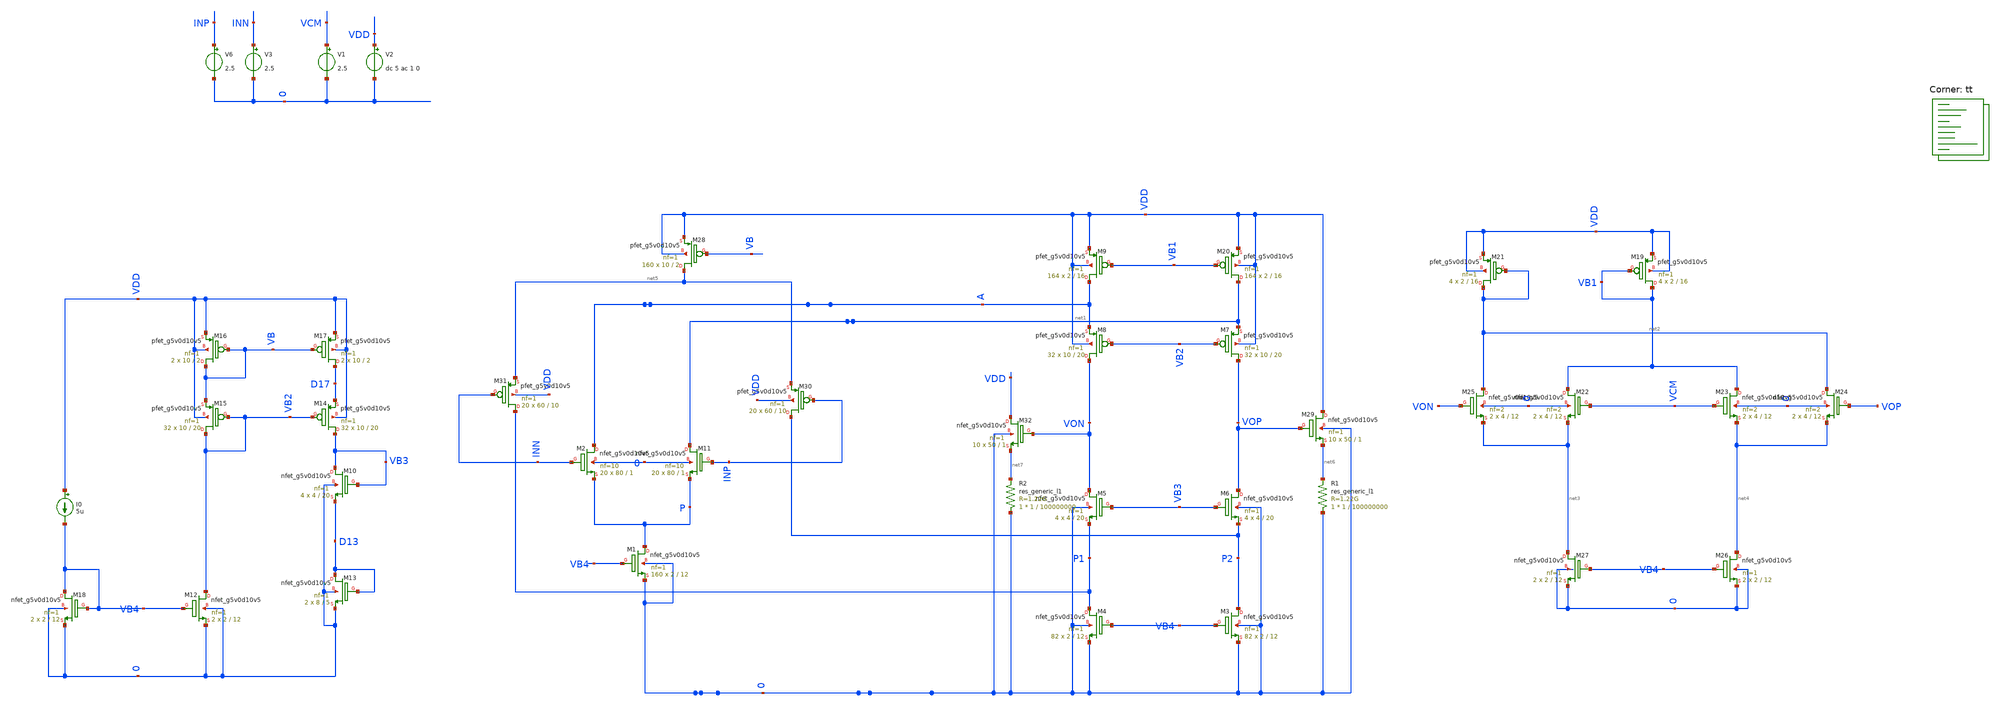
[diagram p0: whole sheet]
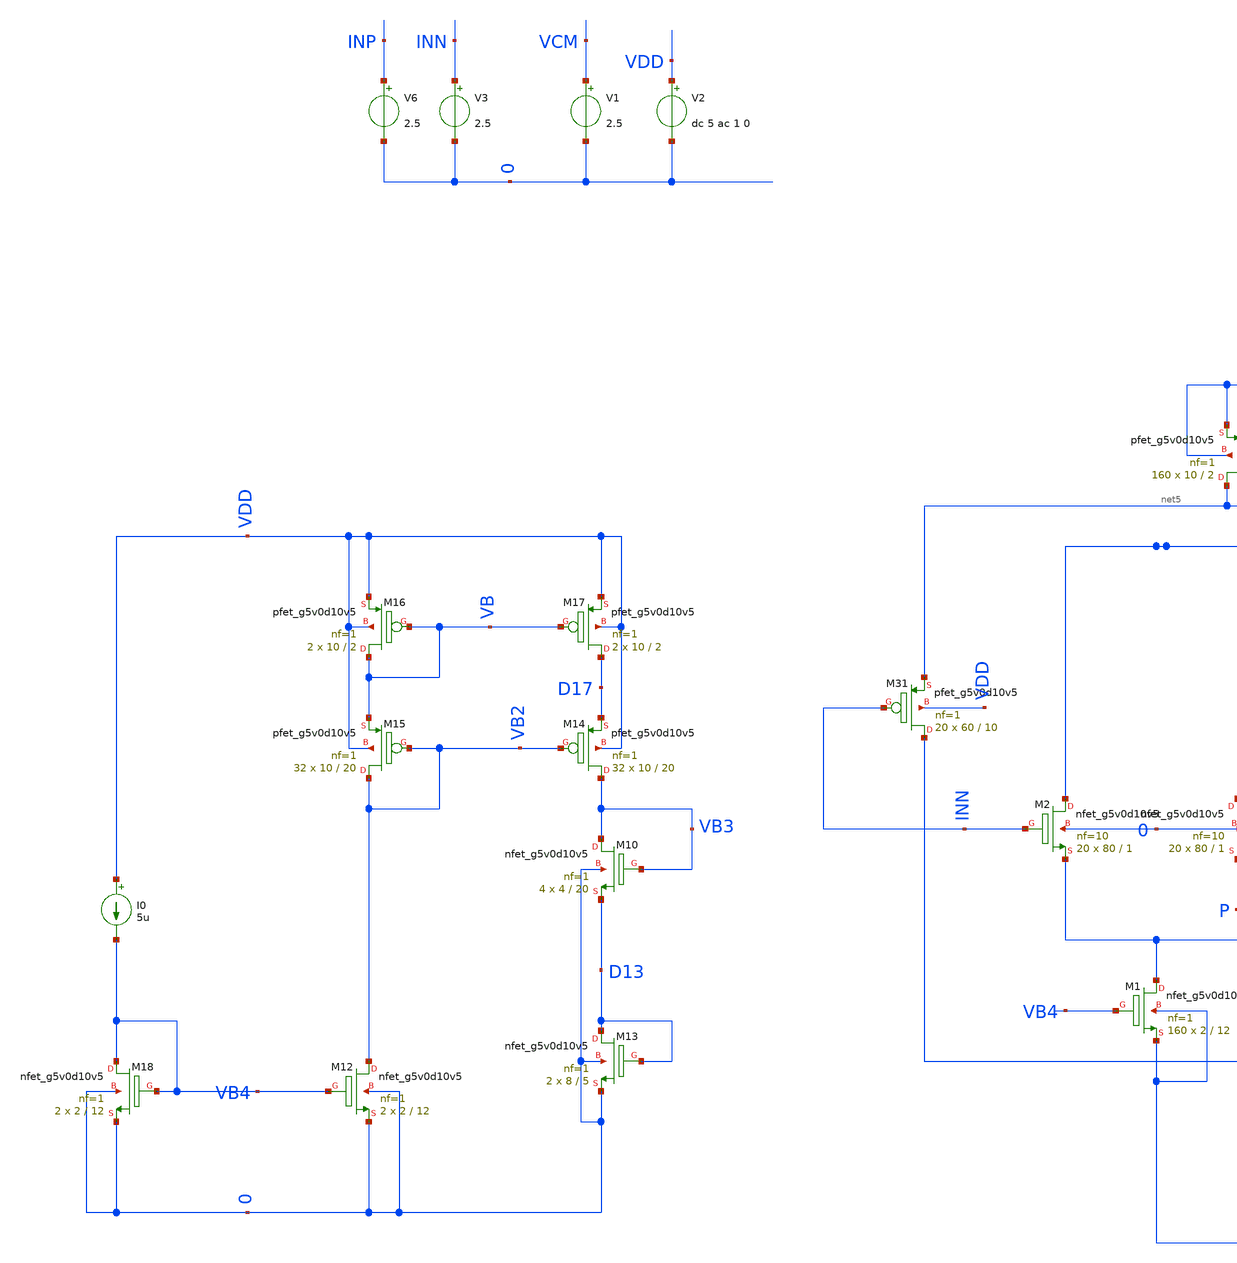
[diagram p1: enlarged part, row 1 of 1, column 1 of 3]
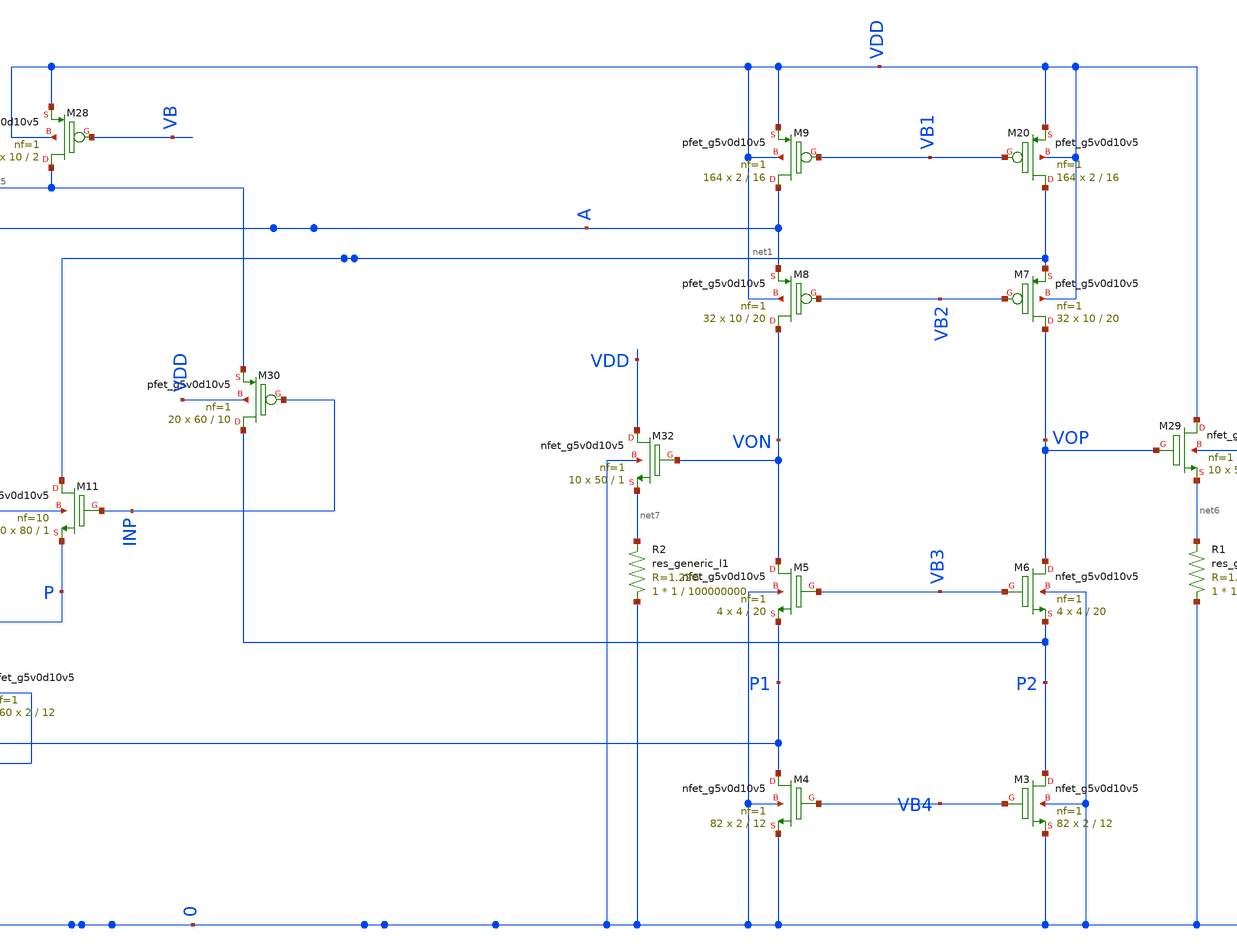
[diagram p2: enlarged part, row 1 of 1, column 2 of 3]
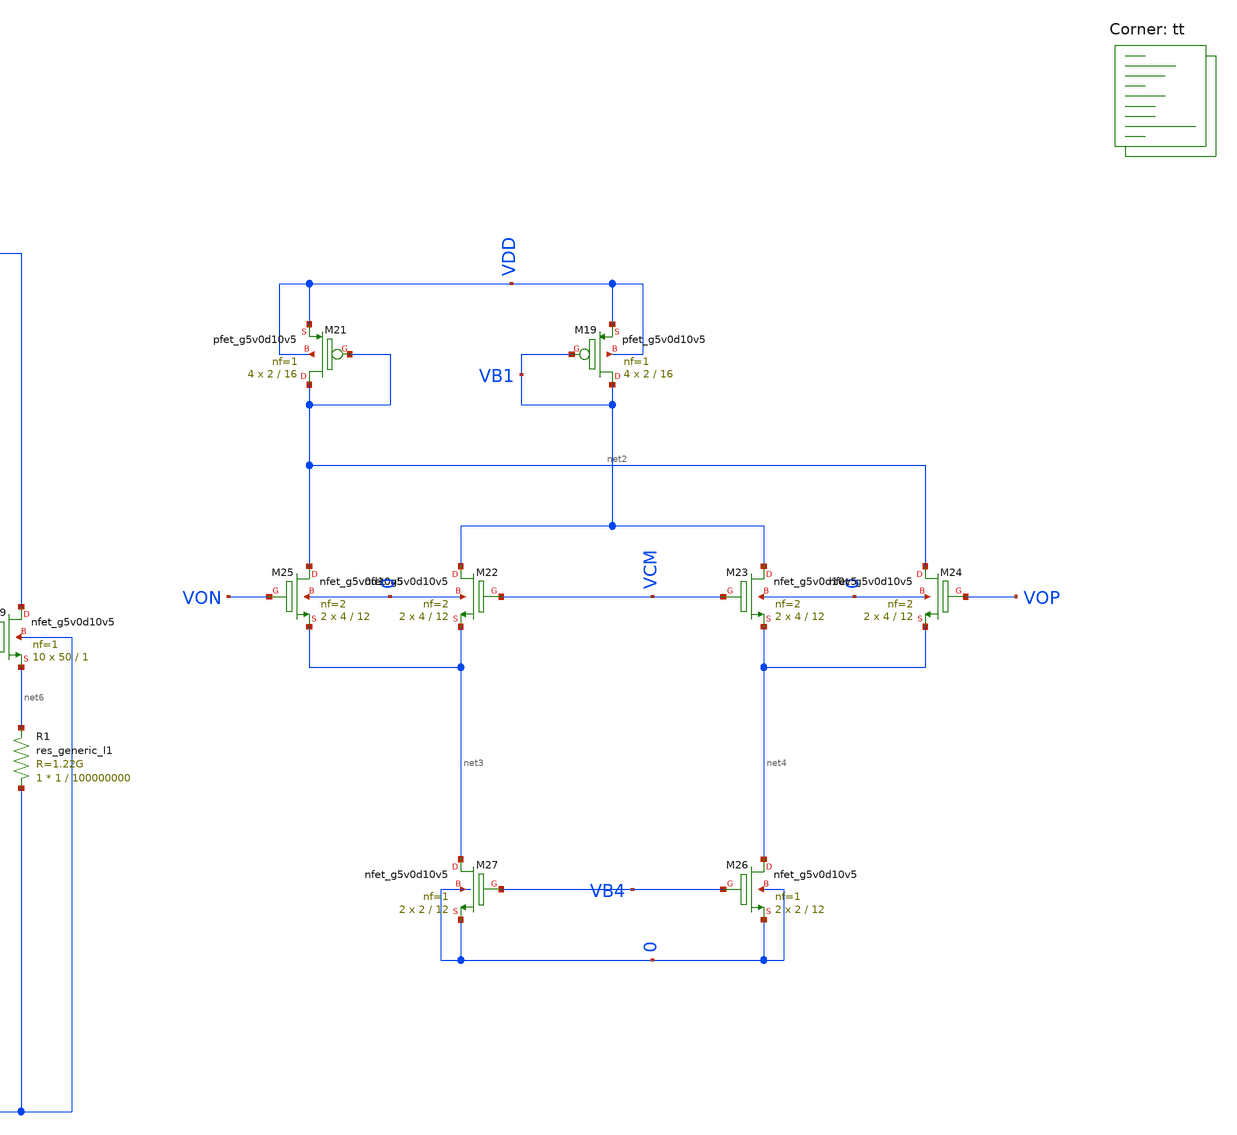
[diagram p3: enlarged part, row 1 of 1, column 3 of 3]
** sch_path: Xschem/tb_PSRR_Folded_5u.sch
**.subckt tb_PSRR_Folded_5u
V6 INP 0 2.5
V1 VCM 0 2.5
V2 VDD 0 dc 5 ac 1 0
V3 INN 0 2.5
I0 VDD VB4 5u
XM13 D13 D13 0 0 sky130_fd_pr__nfet_g5v0d10v5 L=5 W=8 nf=1 ad='int((nf+1)/2) * W/nf * 0.29' as='int((nf+2)/2) * W/nf * 0.29'
+ pd='2*int((nf+1)/2) * (W/nf + 0.29)' ps='2*int((nf+2)/2) * (W/nf + 0.29)' nrd='0.29 / W' nrs='0.29 / W'
+ sa=0 sb=0 sd=0 mult=2 m=2
XM12 VB2 VB4 0 0 sky130_fd_pr__nfet_g5v0d10v5 L=12 W=2 nf=1 ad='int((nf+1)/2) * W/nf * 0.29' as='int((nf+2)/2) * W/nf * 0.29'
+ pd='2*int((nf+1)/2) * (W/nf + 0.29)' ps='2*int((nf+2)/2) * (W/nf + 0.29)' nrd='0.29 / W' nrs='0.29 / W'
+ sa=0 sb=0 sd=0 mult=2 m=2
XM18 VB4 VB4 0 0 sky130_fd_pr__nfet_g5v0d10v5 L=12 W=2 nf=1 ad='int((nf+1)/2) * W/nf * 0.29' as='int((nf+2)/2) * W/nf * 0.29'
+ pd='2*int((nf+1)/2) * (W/nf + 0.29)' ps='2*int((nf+2)/2) * (W/nf + 0.29)' nrd='0.29 / W' nrs='0.29 / W'
+ sa=0 sb=0 sd=0 mult=2 m=2
XM15 VB2 VB2 VB VDD sky130_fd_pr__pfet_g5v0d10v5 L=20 W=10 nf=1 ad='int((nf+1)/2) * W/nf * 0.29' as='int((nf+2)/2) * W/nf * 0.29'
+ pd='2*int((nf+1)/2) * (W/nf + 0.29)' ps='2*int((nf+2)/2) * (W/nf + 0.29)' nrd='0.29 / W' nrs='0.29 / W'
+ sa=0 sb=0 sd=0 mult=32 m=32
XM16 VB VB VDD VDD sky130_fd_pr__pfet_g5v0d10v5 L=2 W=10 nf=1 ad='int((nf+1)/2) * W/nf * 0.29' as='int((nf+2)/2) * W/nf * 0.29'
+ pd='2*int((nf+1)/2) * (W/nf + 0.29)' ps='2*int((nf+2)/2) * (W/nf + 0.29)' nrd='0.29 / W' nrs='0.29 / W'
+ sa=0 sb=0 sd=0 mult=2 m=2
XM17 D17 VB VDD VDD sky130_fd_pr__pfet_g5v0d10v5 L=2 W=10 nf=1 ad='int((nf+1)/2) * W/nf * 0.29' as='int((nf+2)/2) * W/nf * 0.29'
+ pd='2*int((nf+1)/2) * (W/nf + 0.29)' ps='2*int((nf+2)/2) * (W/nf + 0.29)' nrd='0.29 / W' nrs='0.29 / W'
+ sa=0 sb=0 sd=0 mult=2 m=2
XM14 VB3 VB2 D17 VDD sky130_fd_pr__pfet_g5v0d10v5 L=20 W=10 nf=1 ad='int((nf+1)/2) * W/nf * 0.29' as='int((nf+2)/2) * W/nf * 0.29'
+ pd='2*int((nf+1)/2) * (W/nf + 0.29)' ps='2*int((nf+2)/2) * (W/nf + 0.29)' nrd='0.29 / W' nrs='0.29 / W'
+ sa=0 sb=0 sd=0 mult=32 m=32
XM1 P VB4 0 0 sky130_fd_pr__nfet_g5v0d10v5 L=12 W=2 nf=1 ad='int((nf+1)/2) * W/nf * 0.29' as='int((nf+2)/2) * W/nf * 0.29'
+ pd='2*int((nf+1)/2) * (W/nf + 0.29)' ps='2*int((nf+2)/2) * (W/nf + 0.29)' nrd='0.29 / W' nrs='0.29 / W'
+ sa=0 sb=0 sd=0 mult=160 m=160
XM2 A INN P 0 sky130_fd_pr__nfet_g5v0d10v5 L=1 W=80 nf=10 ad='int((nf+1)/2) * W/nf * 0.29' as='int((nf+2)/2) * W/nf * 0.29'
+ pd='2*int((nf+1)/2) * (W/nf + 0.29)' ps='2*int((nf+2)/2) * (W/nf + 0.29)' nrd='0.29 / W' nrs='0.29 / W'
+ sa=0 sb=0 sd=0 mult=20 m=20
XM11 net1 INP P 0 sky130_fd_pr__nfet_g5v0d10v5 L=1 W=80 nf=10 ad='int((nf+1)/2) * W/nf * 0.29' as='int((nf+2)/2) * W/nf * 0.29'
+ pd='2*int((nf+1)/2) * (W/nf + 0.29)' ps='2*int((nf+2)/2) * (W/nf + 0.29)' nrd='0.29 / W' nrs='0.29 / W'
+ sa=0 sb=0 sd=0 mult=20 m=20
XM20 net1 VB1 VDD VDD sky130_fd_pr__pfet_g5v0d10v5 L=16 W=2 nf=1 ad='int((nf+1)/2) * W/nf * 0.29' as='int((nf+2)/2) * W/nf * 0.29'
+ pd='2*int((nf+1)/2) * (W/nf + 0.29)' ps='2*int((nf+2)/2) * (W/nf + 0.29)' nrd='0.29 / W' nrs='0.29 / W'
+ sa=0 sb=0 sd=0 mult=164 m=164
XM9 A VB1 VDD VDD sky130_fd_pr__pfet_g5v0d10v5 L=16 W=2 nf=1 ad='int((nf+1)/2) * W/nf * 0.29' as='int((nf+2)/2) * W/nf * 0.29'
+ pd='2*int((nf+1)/2) * (W/nf + 0.29)' ps='2*int((nf+2)/2) * (W/nf + 0.29)' nrd='0.29 / W' nrs='0.29 / W'
+ sa=0 sb=0 sd=0 mult=164 m=164
XM7 VOP VB2 net1 VDD sky130_fd_pr__pfet_g5v0d10v5 L=20 W=10 nf=1 ad='int((nf+1)/2) * W/nf * 0.29' as='int((nf+2)/2) * W/nf * 0.29'
+ pd='2*int((nf+1)/2) * (W/nf + 0.29)' ps='2*int((nf+2)/2) * (W/nf + 0.29)' nrd='0.29 / W' nrs='0.29 / W'
+ sa=0 sb=0 sd=0 mult=32 m=32
XM8 VON VB2 A VDD sky130_fd_pr__pfet_g5v0d10v5 L=20 W=10 nf=1 ad='int((nf+1)/2) * W/nf * 0.29' as='int((nf+2)/2) * W/nf * 0.29'
+ pd='2*int((nf+1)/2) * (W/nf + 0.29)' ps='2*int((nf+2)/2) * (W/nf + 0.29)' nrd='0.29 / W' nrs='0.29 / W'
+ sa=0 sb=0 sd=0 mult=32 m=32
XM3 P2 VB4 0 0 sky130_fd_pr__nfet_g5v0d10v5 L=12 W=2 nf=1 ad='int((nf+1)/2) * W/nf * 0.29' as='int((nf+2)/2) * W/nf * 0.29'
+ pd='2*int((nf+1)/2) * (W/nf + 0.29)' ps='2*int((nf+2)/2) * (W/nf + 0.29)' nrd='0.29 / W' nrs='0.29 / W'
+ sa=0 sb=0 sd=0 mult=82 m=82
XM4 P1 VB4 0 0 sky130_fd_pr__nfet_g5v0d10v5 L=12 W=2 nf=1 ad='int((nf+1)/2) * W/nf * 0.29' as='int((nf+2)/2) * W/nf * 0.29'
+ pd='2*int((nf+1)/2) * (W/nf + 0.29)' ps='2*int((nf+2)/2) * (W/nf + 0.29)' nrd='0.29 / W' nrs='0.29 / W'
+ sa=0 sb=0 sd=0 mult=82 m=82
XM5 VON VB3 P1 0 sky130_fd_pr__nfet_g5v0d10v5 L=20 W=4 nf=1 ad='int((nf+1)/2) * W/nf * 0.29' as='int((nf+2)/2) * W/nf * 0.29'
+ pd='2*int((nf+1)/2) * (W/nf + 0.29)' ps='2*int((nf+2)/2) * (W/nf + 0.29)' nrd='0.29 / W' nrs='0.29 / W'
+ sa=0 sb=0 sd=0 mult=4 m=4
XM6 VOP VB3 P2 0 sky130_fd_pr__nfet_g5v0d10v5 L=20 W=4 nf=1 ad='int((nf+1)/2) * W/nf * 0.29' as='int((nf+2)/2) * W/nf * 0.29'
+ pd='2*int((nf+1)/2) * (W/nf + 0.29)' ps='2*int((nf+2)/2) * (W/nf + 0.29)' nrd='0.29 / W' nrs='0.29 / W'
+ sa=0 sb=0 sd=0 mult=4 m=4
XM10 VB3 VB3 D13 0 sky130_fd_pr__nfet_g5v0d10v5 L=20 W=4 nf=1 ad='int((nf+1)/2) * W/nf * 0.29' as='int((nf+2)/2) * W/nf * 0.29'
+ pd='2*int((nf+1)/2) * (W/nf + 0.29)' ps='2*int((nf+2)/2) * (W/nf + 0.29)' nrd='0.29 / W' nrs='0.29 / W'
+ sa=0 sb=0 sd=0 mult=4 m=4
XM19 VB1 VB1 VDD VDD sky130_fd_pr__pfet_g5v0d10v5 L=16 W=2 nf=1 ad='int((nf+1)/2) * W/nf * 0.29' as='int((nf+2)/2) * W/nf * 0.29'
+ pd='2*int((nf+1)/2) * (W/nf + 0.29)' ps='2*int((nf+2)/2) * (W/nf + 0.29)' nrd='0.29 / W' nrs='0.29 / W'
+ sa=0 sb=0 sd=0 mult=4 m=4
XM21 net2 net2 VDD VDD sky130_fd_pr__pfet_g5v0d10v5 L=16 W=2 nf=1 ad='int((nf+1)/2) * W/nf * 0.29' as='int((nf+2)/2) * W/nf * 0.29'
+ pd='2*int((nf+1)/2) * (W/nf + 0.29)' ps='2*int((nf+2)/2) * (W/nf + 0.29)' nrd='0.29 / W' nrs='0.29 / W'
+ sa=0 sb=0 sd=0 mult=4 m=4
XM22 VB1 VCM net3 0 sky130_fd_pr__nfet_g5v0d10v5 L=12 W=4 nf=2 ad='int((nf+1)/2) * W/nf * 0.29' as='int((nf+2)/2) * W/nf * 0.29'
+ pd='2*int((nf+1)/2) * (W/nf + 0.29)' ps='2*int((nf+2)/2) * (W/nf + 0.29)' nrd='0.29 / W' nrs='0.29 / W'
+ sa=0 sb=0 sd=0 mult=2 m=2
XM24 net2 VOP net4 0 sky130_fd_pr__nfet_g5v0d10v5 L=12 W=4 nf=2 ad='int((nf+1)/2) * W/nf * 0.29' as='int((nf+2)/2) * W/nf * 0.29'
+ pd='2*int((nf+1)/2) * (W/nf + 0.29)' ps='2*int((nf+2)/2) * (W/nf + 0.29)' nrd='0.29 / W' nrs='0.29 / W'
+ sa=0 sb=0 sd=0 mult=2 m=2
XM25 net2 VON net3 0 sky130_fd_pr__nfet_g5v0d10v5 L=12 W=4 nf=2 ad='int((nf+1)/2) * W/nf * 0.29' as='int((nf+2)/2) * W/nf * 0.29'
+ pd='2*int((nf+1)/2) * (W/nf + 0.29)' ps='2*int((nf+2)/2) * (W/nf + 0.29)' nrd='0.29 / W' nrs='0.29 / W'
+ sa=0 sb=0 sd=0 mult=2 m=2
XM26 net4 VB4 0 0 sky130_fd_pr__nfet_g5v0d10v5 L=12 W=2 nf=1 ad='int((nf+1)/2) * W/nf * 0.29' as='int((nf+2)/2) * W/nf * 0.29'
+ pd='2*int((nf+1)/2) * (W/nf + 0.29)' ps='2*int((nf+2)/2) * (W/nf + 0.29)' nrd='0.29 / W' nrs='0.29 / W'
+ sa=0 sb=0 sd=0 mult=2 m=2
XM27 net3 VB4 0 0 sky130_fd_pr__nfet_g5v0d10v5 L=12 W=2 nf=1 ad='int((nf+1)/2) * W/nf * 0.29' as='int((nf+2)/2) * W/nf * 0.29'
+ pd='2*int((nf+1)/2) * (W/nf + 0.29)' ps='2*int((nf+2)/2) * (W/nf + 0.29)' nrd='0.29 / W' nrs='0.29 / W'
+ sa=0 sb=0 sd=0 mult=2 m=2
XM23 VB1 VCM net4 0 sky130_fd_pr__nfet_g5v0d10v5 L=12 W=4 nf=2 ad='int((nf+1)/2) * W/nf * 0.29' as='int((nf+2)/2) * W/nf * 0.29'
+ pd='2*int((nf+1)/2) * (W/nf + 0.29)' ps='2*int((nf+2)/2) * (W/nf + 0.29)' nrd='0.29 / W' nrs='0.29 / W'
+ sa=0 sb=0 sd=0 mult=2 m=2
XM30 P2 INP net5 VDD sky130_fd_pr__pfet_g5v0d10v5 L=10 W=60 nf=1 ad='int((nf+1)/2) * W/nf * 0.29' as='int((nf+2)/2) * W/nf * 0.29'
+ pd='2*int((nf+1)/2) * (W/nf + 0.29)' ps='2*int((nf+2)/2) * (W/nf + 0.29)' nrd='0.29 / W' nrs='0.29 / W'
+ sa=0 sb=0 sd=0 mult=20 m=20
XM31 P1 INN net5 VDD sky130_fd_pr__pfet_g5v0d10v5 L=10 W=60 nf=1 ad='int((nf+1)/2) * W/nf * 0.29' as='int((nf+2)/2) * W/nf * 0.29'
+ pd='2*int((nf+1)/2) * (W/nf + 0.29)' ps='2*int((nf+2)/2) * (W/nf + 0.29)' nrd='0.29 / W' nrs='0.29 / W'
+ sa=0 sb=0 sd=0 mult=20 m=20
XM28 net5 VB VDD VDD sky130_fd_pr__pfet_g5v0d10v5 L=2 W=10 nf=1 ad='int((nf+1)/2) * W/nf * 0.29' as='int((nf+2)/2) * W/nf * 0.29'
+ pd='2*int((nf+1)/2) * (W/nf + 0.29)' ps='2*int((nf+2)/2) * (W/nf + 0.29)' nrd='0.29 / W' nrs='0.29 / W'
+ sa=0 sb=0 sd=0 mult=160 m=160
XM29 VDD VOP net6 0 sky130_fd_pr__nfet_g5v0d10v5 L=1 W=50 nf=1 ad='int((nf+1)/2) * W/nf * 0.29' as='int((nf+2)/2) * W/nf * 0.29'
+ pd='2*int((nf+1)/2) * (W/nf + 0.29)' ps='2*int((nf+2)/2) * (W/nf + 0.29)' nrd='0.29 / W' nrs='0.29 / W'
+ sa=0 sb=0 sd=0 mult=10 m=10
R1 0 net6 sky130_fd_pr__res_generic_l1 W=1 L=100000000 m=1
XM32 VDD VON net7 0 sky130_fd_pr__nfet_g5v0d10v5 L=1 W=50 nf=1 ad='int((nf+1)/2) * W/nf * 0.29' as='int((nf+2)/2) * W/nf * 0.29'
+ pd='2*int((nf+1)/2) * (W/nf + 0.29)' ps='2*int((nf+2)/2) * (W/nf + 0.29)' nrd='0.29 / W' nrs='0.29 / W'
+ sa=0 sb=0 sd=0 mult=10 m=10
R2 0 net7 sky130_fd_pr__res_generic_l1 W=1 L=100000000 m=1
**** begin user architecture code
.lib $::SKYWATER_MODELS/sky130.lib.spice tt

* this option enables mos model bin
* selection based on W/NF instead of W
.option wnflag=1
.option savecurrents

.control
save all
save @m.xm15.msky130_fd_pr__pfet_g5v0d10v5[vth]
save @m.xm15.msky130_fd_pr__pfet_g5v0d10v5[gm]
save @m.xm9.msky130_fd_pr__pfet_g5v0d10v5[vth]
save @m.xm9.msky130_fd_pr__pfet_g5v0d10v5[gm]
save @m.xm8.msky130_fd_pr__pfet_g5v0d10v5[vth]
save @m.xm8.msky130_fd_pr__pfet_g5v0d10v5[gm]
save @m.xm20.msky130_fd_pr__pfet_g5v0d10v5[vth]
save @m.xm20.msky130_fd_pr__pfet_g5v0d10v5[gm]
save @m.xm7.msky130_fd_pr__pfet_g5v0d10v5[vth]
save @m.xm7.msky130_fd_pr__pfet_g5v0d10v5[gm]
save @m.xm10.msky130_fd_pr__nfet_g5v0d10v5[gm]
save @m.xm10.msky130_fd_pr__nfet_g5v0d10v5[vth]
save @m.xm14.msky130_fd_pr__pfet_g5v0d10v5[gm]
save @m.xm14.msky130_fd_pr__pfet_g5v0d10v5[vth]
save @m.xm16.msky130_fd_pr__pfet_g5v0d10v5[gm]
save @m.xm16.msky130_fd_pr__pfet_g5v0d10v5[vth]
save @m.xm17.msky130_fd_pr__pfet_g5v0d10v5[gm]
save @m.xm17.msky130_fd_pr__pfet_g5v0d10v5[vth]
save @m.xm13.msky130_fd_pr__nfet_g5v0d10v5[gm]
save @m.xm13.msky130_fd_pr__nfet_g5v0d10v5[vth]
save @m.xm12.msky130_fd_pr__nfet_g5v0d10v5[vth]
save @m.xm18.msky130_fd_pr__nfet_g5v0d10v5[vth]
*folded
save @m.xm2.msky130_fd_pr__nfet_g5v0d10v5[vth]
save @m.xm11.msky130_fd_pr__nfet_g5v0d10v5[vth]
save @m.xm1.msky130_fd_pr__nfet_g5v0d10v5[vth]
save @m.xm5.msky130_fd_pr__nfet_g5v0d10v5[vth]
save @m.xm6.msky130_fd_pr__nfet_g5v0d10v5[vth]
save @m.xm4.msky130_fd_pr__nfet_g5v0d10v5[vth]
save @m.xm3.msky130_fd_pr__nfet_g5v0d10v5[vth]
save @m.xm7.msky130_fd_pr__pfet_g5v0d10v5[vth]
save @m.xm8.msky130_fd_pr__pfet_g5v0d10v5[vth]
save @m.xm9.msky130_fd_pr__pfet_g5v0d10v5[vth]
save @m.xm20.msky130_fd_pr__pfet_g5v0d10v5[vth]
*CMFB
save @m.xm21.msky130_fd_pr__pfet_g5v0d10v5[vth]
save @m.xm19.msky130_fd_pr__pfet_g5v0d10v5[vth]
save @m.xm22.msky130_fd_pr__nfet_g5v0d10v5[vth]
save @m.xm23.msky130_fd_pr__nfet_g5v0d10v5[vth]
save @m.xm25.msky130_fd_pr__nfet_g5v0d10v5[vth]
save @m.xm27.msky130_fd_pr__nfet_g5v0d10v5[vth]
save @m.xm26.msky130_fd_pr__nfet_g5v0d10v5[vth]
save @m.xm24.msky130_fd_pr__nfet_g5v0d10v5[vth]
save current


write Folded_5u.raw

op
print VON VOP VB2 VB
*print @m.xm18.msky130_fd_pr__nfet_g5v0d10v5
*print @m.xm12.msky130_fd_pr__nfet_g5v0d10v5
*print @m.xm13.msky130_fd_pr__nfet_g5v0d10v5
*print @m.xm10.msky130_fd_pr__nfet_g5v0d10v5
*print @m.xm14.msky130_fd_pr__pfet_g5v0d10v5
*print @m.xm17.msky130_fd_pr__pfet_g5v0d10v5
*print @m.xm15.msky130_fd_pr__pfet_g5v0d10v5
*print @m.xm16.msky130_fd_pr__pfet_g5v0d10v5
*Folded cascode
*print @m.xm9.msky130_fd_pr__pfet_g5v0d10v5
*print @m.xm8.msky130_fd_pr__pfet_g5v0d10v5
*print @m.xm5.msky130_fd_pr__nfet_g5v0d10v5
*print @m.xm4.msky130_fd_pr__nfet_g5v0d10v5
*print @m.xm1.msky130_fd_pr__nfet_g5v0d10v5
*print @m.xm2.msky130_fd_pr__nfet_g5v0d10v5
*print @m.xm11.msky130_fd_pr__nfet_g5v0d10v5
*CMFB
print @m.xm23.msky130_fd_pr__nfet_g5v0d10v5
print @m.xm24.msky130_fd_pr__nfet_g5v0d10v5
print @m.xm25.msky130_fd_pr__nfet_g5v0d10v5
print @m.xm22.msky130_fd_pr__nfet_g5v0d10v5
*print @m.xm9.msky130_fd_pr__pfet_g5v0d10v5
*print @m.xm8.msky130_fd_pr__pfet_g5v0d10v5
*print @m.xm4.msky130_fd_pr__nfet_g5v0d10v5
*print @m.xm5.msky130_fd_pr__nfet_g5v0d10v5
print @m.xm28.msky130_fd_pr__pfet_g5v0d10v5
*print @m.xm26.msky130_fd_pr__nfet_g5v0d10v5
*print @m.xm27.msky130_fd_pr__nfet_g5v0d10v5
print @m.xm30.msky130_fd_pr__pfet_g5v0d10v5
print @m.xm31.msky130_fd_pr__pfet_g5v0d10v5
write Folded_5u.raw
ac dec 10 1 1e9
  remzerovec
  write Folded_5u.raw
trans 1u 1m
quit 0
.endc


**** end user architecture code
**.ends
.end
